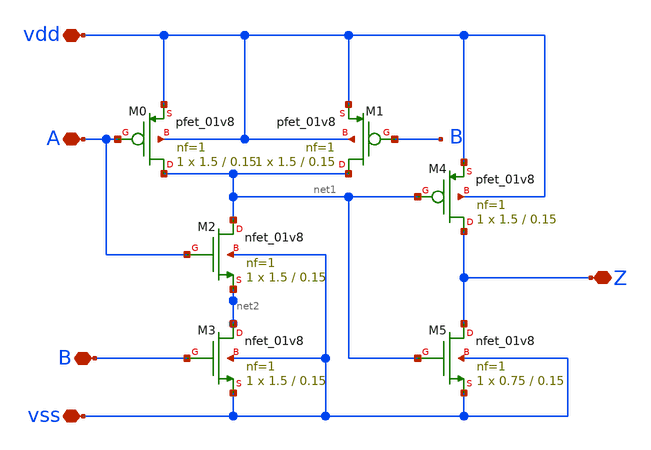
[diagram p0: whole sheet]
** sch_path: sch/andgate.sch
**.subckt andgate vdd Z A B vss
*.iopin vdd
*.iopin Z
*.iopin A
*.iopin B
*.iopin vss
XM0 net1 A vdd vdd sky130_fd_pr__pfet_01v8 L=0.15 W=1.5 nf=1 ad='int((nf+1)/2) * W/nf * 0.29' as='int((nf+2)/2) * W/nf * 0.29'
+ pd='2*int((nf+1)/2) * (W/nf + 0.29)' ps='2*int((nf+2)/2) * (W/nf + 0.29)' nrd='0.29 / W' nrs='0.29 / W'
+ sa=0 sb=0 sd=0 mult=1 m=1
XM2 net1 A net2 vss sky130_fd_pr__nfet_01v8 L=0.15 W=1.5 nf=1 ad='int((nf+1)/2) * W/nf * 0.29' as='int((nf+2)/2) * W/nf * 0.29'
+ pd='2*int((nf+1)/2) * (W/nf + 0.29)' ps='2*int((nf+2)/2) * (W/nf + 0.29)' nrd='0.29 / W' nrs='0.29 / W'
+ sa=0 sb=0 sd=0 mult=1 m=1
XM3 net2 B vss vss sky130_fd_pr__nfet_01v8 L=0.15 W=1.5 nf=1 ad='int((nf+1)/2) * W/nf * 0.29' as='int((nf+2)/2) * W/nf * 0.29'
+ pd='2*int((nf+1)/2) * (W/nf + 0.29)' ps='2*int((nf+2)/2) * (W/nf + 0.29)' nrd='0.29 / W' nrs='0.29 / W'
+ sa=0 sb=0 sd=0 mult=1 m=1
XM4 Z net1 vdd vdd sky130_fd_pr__pfet_01v8 L=0.15 W=1.5 nf=1 ad='int((nf+1)/2) * W/nf * 0.29' as='int((nf+2)/2) * W/nf * 0.29'
+ pd='2*int((nf+1)/2) * (W/nf + 0.29)' ps='2*int((nf+2)/2) * (W/nf + 0.29)' nrd='0.29 / W' nrs='0.29 / W'
+ sa=0 sb=0 sd=0 mult=1 m=1
XM5 Z net1 vss vss sky130_fd_pr__nfet_01v8 L=0.15 W=0.75 nf=1 ad='int((nf+1)/2) * W/nf * 0.29' as='int((nf+2)/2) * W/nf * 0.29'
+ pd='2*int((nf+1)/2) * (W/nf + 0.29)' ps='2*int((nf+2)/2) * (W/nf + 0.29)' nrd='0.29 / W' nrs='0.29 / W'
+ sa=0 sb=0 sd=0 mult=1 m=1
XM1 net1 B vdd vdd sky130_fd_pr__pfet_01v8 L=0.15 W=1.5 nf=1 ad='int((nf+1)/2) * W/nf * 0.29' as='int((nf+2)/2) * W/nf * 0.29'
+ pd='2*int((nf+1)/2) * (W/nf + 0.29)' ps='2*int((nf+2)/2) * (W/nf + 0.29)' nrd='0.29 / W' nrs='0.29 / W'
+ sa=0 sb=0 sd=0 mult=1 m=1
**.ends
.end
